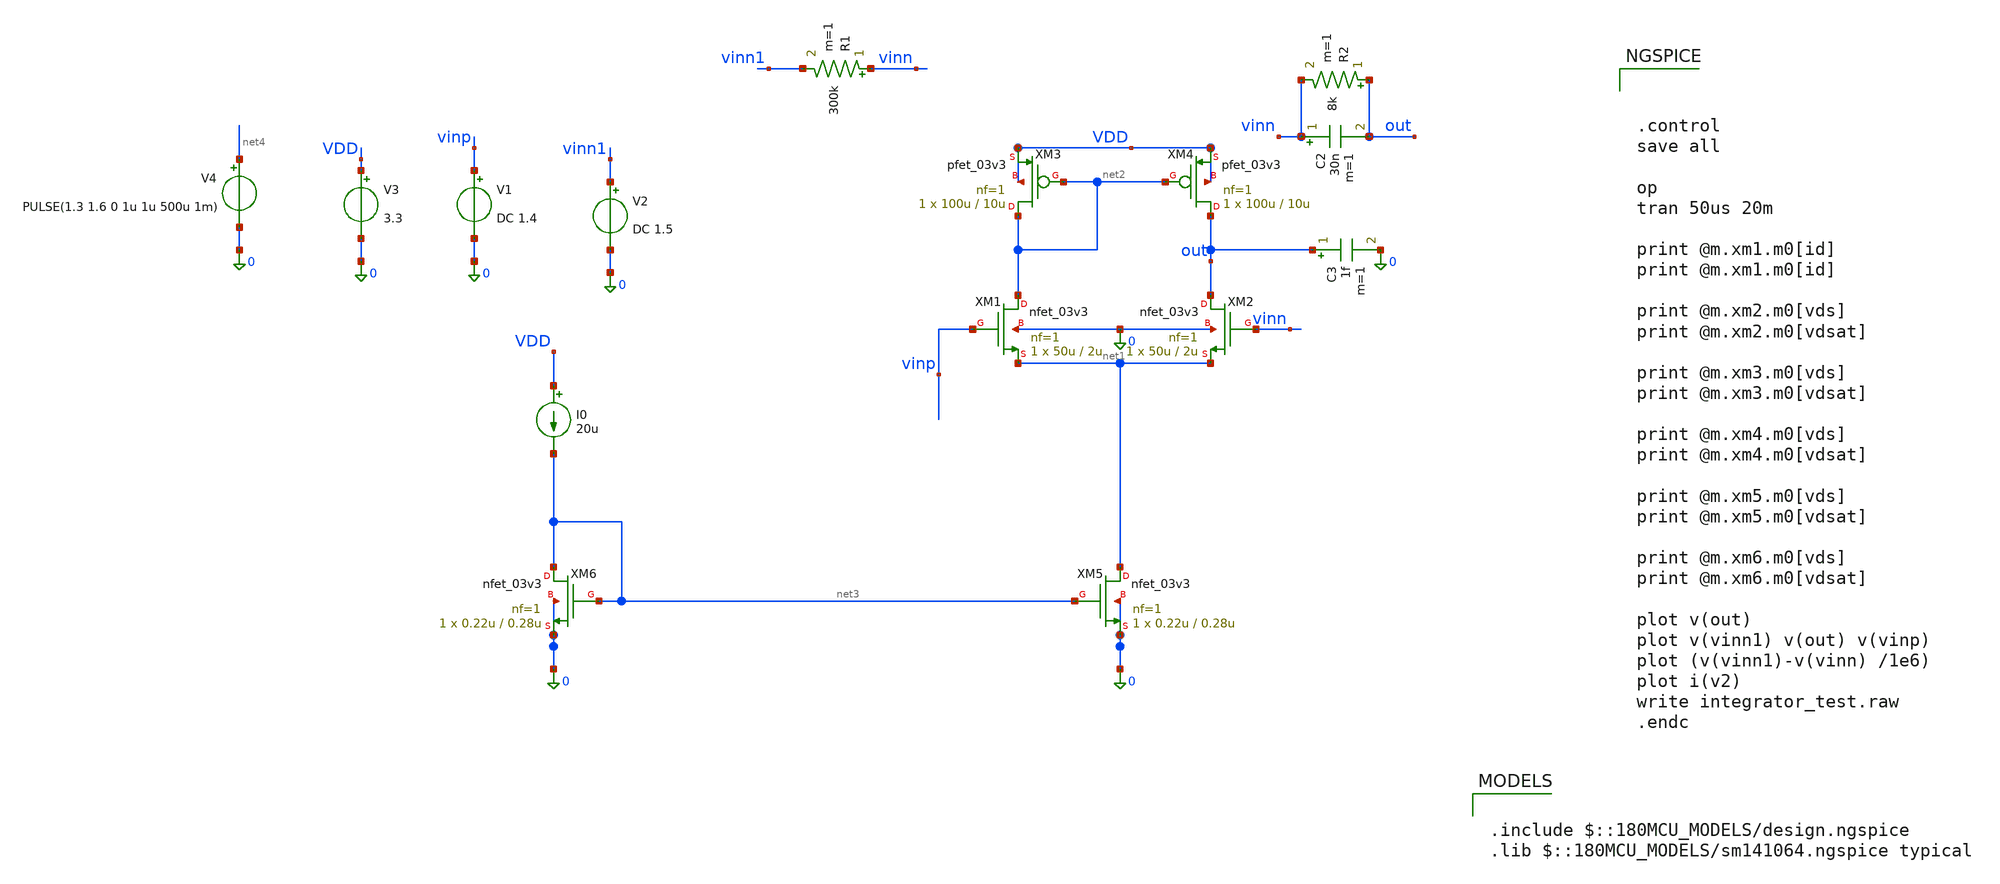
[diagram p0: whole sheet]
** sch_path: amplifier/integrator_test.sch
**.subckt integrator_test
XM1 net2 vinp net1 0 nfet_03v3 L=2u W=50u nf=1 ad='int((nf+1)/2) * W/nf * 0.18u' as='int((nf+2)/2) * W/nf * 0.18u'
+ pd='2*int((nf+1)/2) * (W/nf + 0.18u)' ps='2*int((nf+2)/2) * (W/nf + 0.18u)' nrd='0.18u / W' nrs='0.18u / W'
+ sa=0 sb=0 sd=0 m=1
XM2 out vinn net1 0 nfet_03v3 L=2u W=50u nf=1 ad='int((nf+1)/2) * W/nf * 0.18u' as='int((nf+2)/2) * W/nf * 0.18u'
+ pd='2*int((nf+1)/2) * (W/nf + 0.18u)' ps='2*int((nf+2)/2) * (W/nf + 0.18u)' nrd='0.18u / W' nrs='0.18u / W'
+ sa=0 sb=0 sd=0 m=1
XM3 net2 net2 VDD VDD pfet_03v3 L=10u W=100u nf=1 ad='int((nf+1)/2) * W/nf * 0.18u' as='int((nf+2)/2) * W/nf * 0.18u'
+ pd='2*int((nf+1)/2) * (W/nf + 0.18u)' ps='2*int((nf+2)/2) * (W/nf + 0.18u)' nrd='0.18u / W' nrs='0.18u / W'
+ sa=0 sb=0 sd=0 m=1
XM4 out net2 VDD VDD pfet_03v3 L=10u W=100u nf=1 ad='int((nf+1)/2) * W/nf * 0.18u' as='int((nf+2)/2) * W/nf * 0.18u'
+ pd='2*int((nf+1)/2) * (W/nf + 0.18u)' ps='2*int((nf+2)/2) * (W/nf + 0.18u)' nrd='0.18u / W' nrs='0.18u / W'
+ sa=0 sb=0 sd=0 m=1
XM5 net1 net3 0 0 nfet_03v3 L=0.28u W=0.22u nf=1 ad='int((nf+1)/2) * W/nf * 0.18u' as='int((nf+2)/2) * W/nf * 0.18u'
+ pd='2*int((nf+1)/2) * (W/nf + 0.18u)' ps='2*int((nf+2)/2) * (W/nf + 0.18u)' nrd='0.18u / W' nrs='0.18u / W'
+ sa=0 sb=0 sd=0 m=1
XM6 net3 net3 0 0 nfet_03v3 L=0.28u W=0.22u nf=1 ad='int((nf+1)/2) * W/nf * 0.18u' as='int((nf+2)/2) * W/nf * 0.18u'
+ pd='2*int((nf+1)/2) * (W/nf + 0.18u)' ps='2*int((nf+2)/2) * (W/nf + 0.18u)' nrd='0.18u / W' nrs='0.18u / W'
+ sa=0 sb=0 sd=0 m=1
V1 vinp 0 DC 1.4
V3 VDD 0 3.3
I0 VDD net3 20u
C2 vinn out 30n m=1
R1 vinn vinn1 300k m=1
V4 net4 0 PULSE(1.3 1.6 0 1u 1u 500u 1m)
C3 out 0 1f m=1
R2 out vinn 8k m=1
V2 vinn1 0 DC 1.5
**** begin user architecture code

.include $::180MCU_MODELS/design.ngspice
.lib $::180MCU_MODELS/sm141064.ngspice typical




.control
save all

op
tran 50us 20m

print @m.xm1.m0[id]
print @m.xm1.m0[id]

print @m.xm2.m0[vds]
print @m.xm2.m0[vdsat]

print @m.xm3.m0[vds]
print @m.xm3.m0[vdsat]

print @m.xm4.m0[vds]
print @m.xm4.m0[vdsat]

print @m.xm5.m0[vds]
print @m.xm5.m0[vdsat]

print @m.xm6.m0[vds]
print @m.xm6.m0[vdsat]

plot v(out)
plot v(vinn1) v(out) v(vinp)
plot (v(vinn1)-v(vinn) /1e6)
plot i(v2)
write integrator_test.raw
.endc


**** end user architecture code
**.ends
.end
